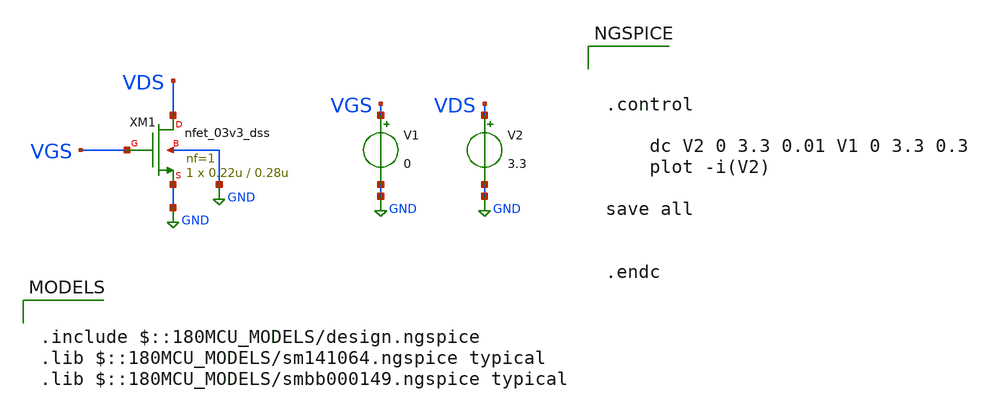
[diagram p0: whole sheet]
** sch_path: week01_mosfet_cmos/tugas1_iv_curve/mosfet-iv-characteristics.sch
**.subckt mosfet-iv-characteristics
V1 VGS GND 0
V2 VDS GND 3.3
XM1 VDS VGS GND GND nfet_03v3_dss L=0.28u W=0.22u nf=1 ad='int((nf+1)/2) * W/nf * 0.18u' as='int((nf+2)/2) * W/nf * 0.18u'
+ pd='2*int((nf+1)/2) * (W/nf + 0.18u)' ps='2*int((nf+2)/2) * (W/nf + 0.18u)' nrd='0.18u / W' nrs='0.18u / W'
+ sa=0 sb=0 sd=0 m=1
**** begin user architecture code

.include $::180MCU_MODELS/design.ngspice
.lib $::180MCU_MODELS/sm141064.ngspice typical
.lib $::180MCU_MODELS/smbb000149.ngspice typical




.control

	dc V2 0 3.3 0.01 V1 0 3.3 0.3
	plot -i(V2)

save all


.endc


**** end user architecture code
**.ends
.GLOBAL GND
.end
